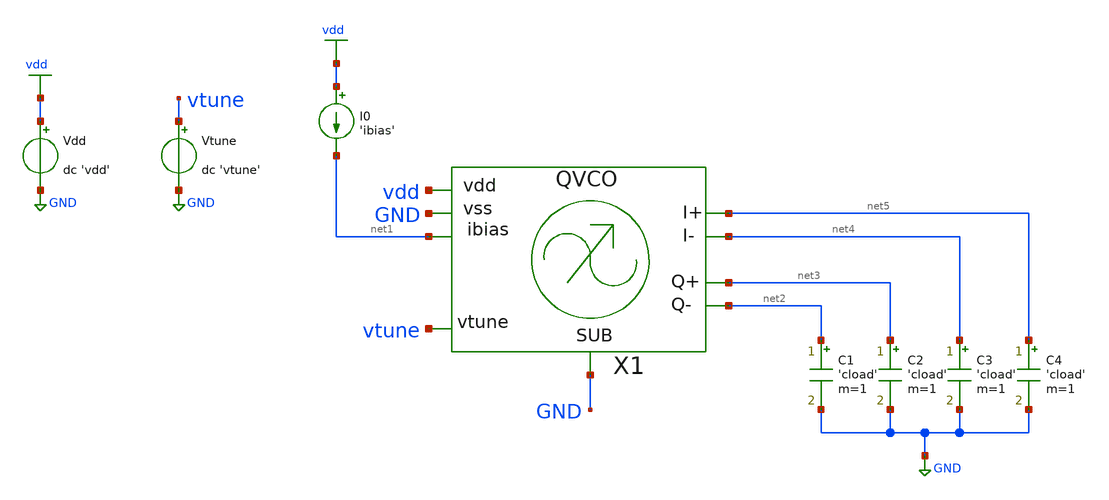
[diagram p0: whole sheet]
** sch_path: tb/vco/tb_op.sch
**.subckt tb_op
Vdd vdd GND dc 'vdd'
Vtune vtune GND dc 'vtune'
X1 vdd GND vtune net5 net4 net3 net2 GND net1 vco m=1
I0 vdd net1 'ibias'
C1 net2 GND 'cload' m=1
C2 net3 GND 'cload' m=1
C3 net4 GND 'cload' m=1
C4 net5 GND 'cload' m=1
**** begin user architecture code


.include 'models_dir'/design.spice
.lib 'models_dir'/sm141064.spice 'mos_corner'
.lib 'models_dir'/sm141064.spice moscap_'mos_corner'
.lib 'models_dir'/sm141064.spice moscap
.option TEMP='temperature'
.option warn=1
.option savecurrents
.control
save all
op
print I(Vmeas_vdd)
set wr_singlescale
wrdata 'simpath'/'filename'_'N'.data -I(Vmeas_vdd)
set filetype=ascii
write 'simpath'/'filename'_'N'.raw
quit
.endc


**** end user architecture code
**.ends
.GLOBAL GND
.GLOBAL vdd
.end
